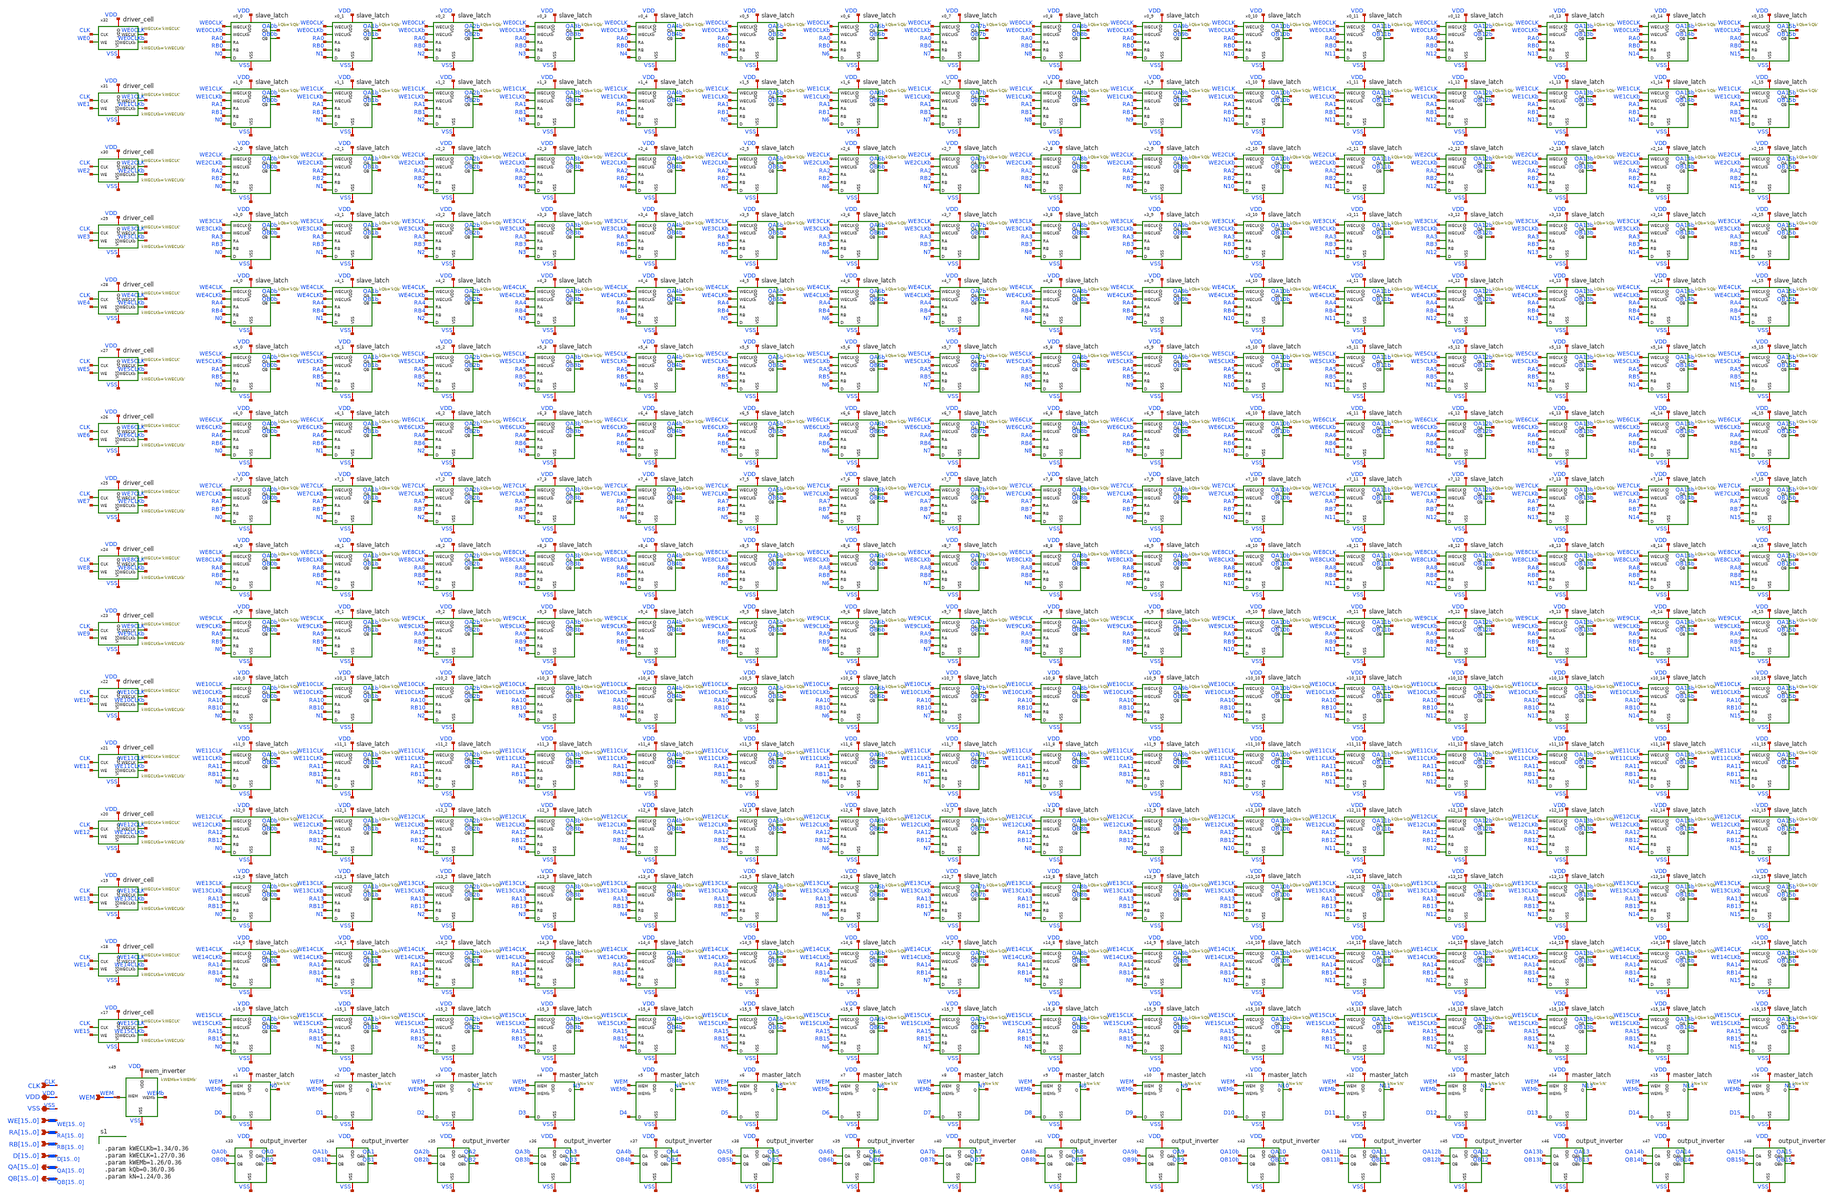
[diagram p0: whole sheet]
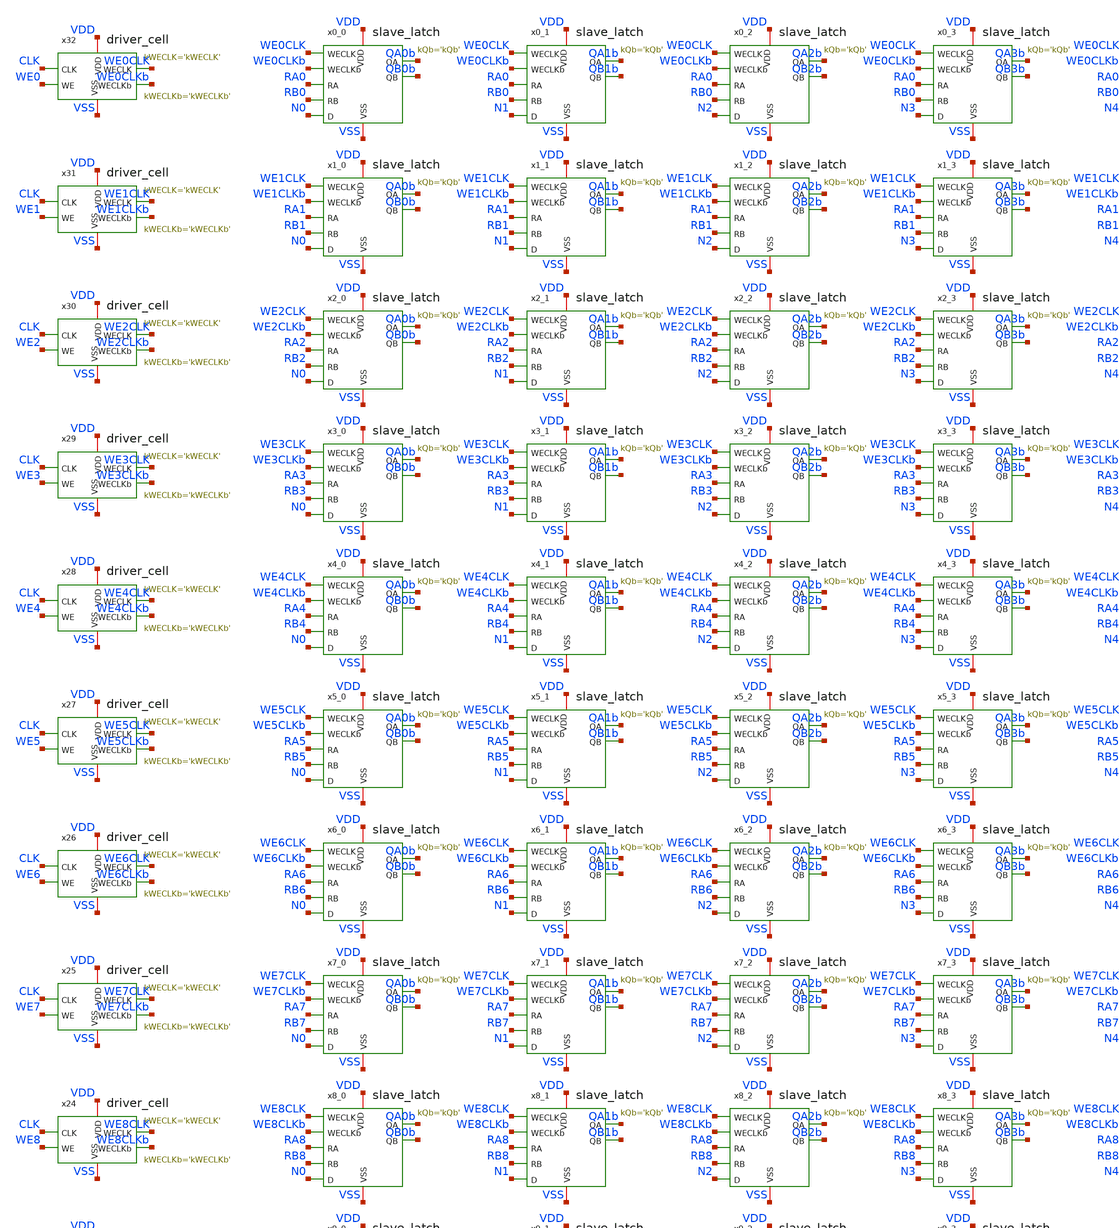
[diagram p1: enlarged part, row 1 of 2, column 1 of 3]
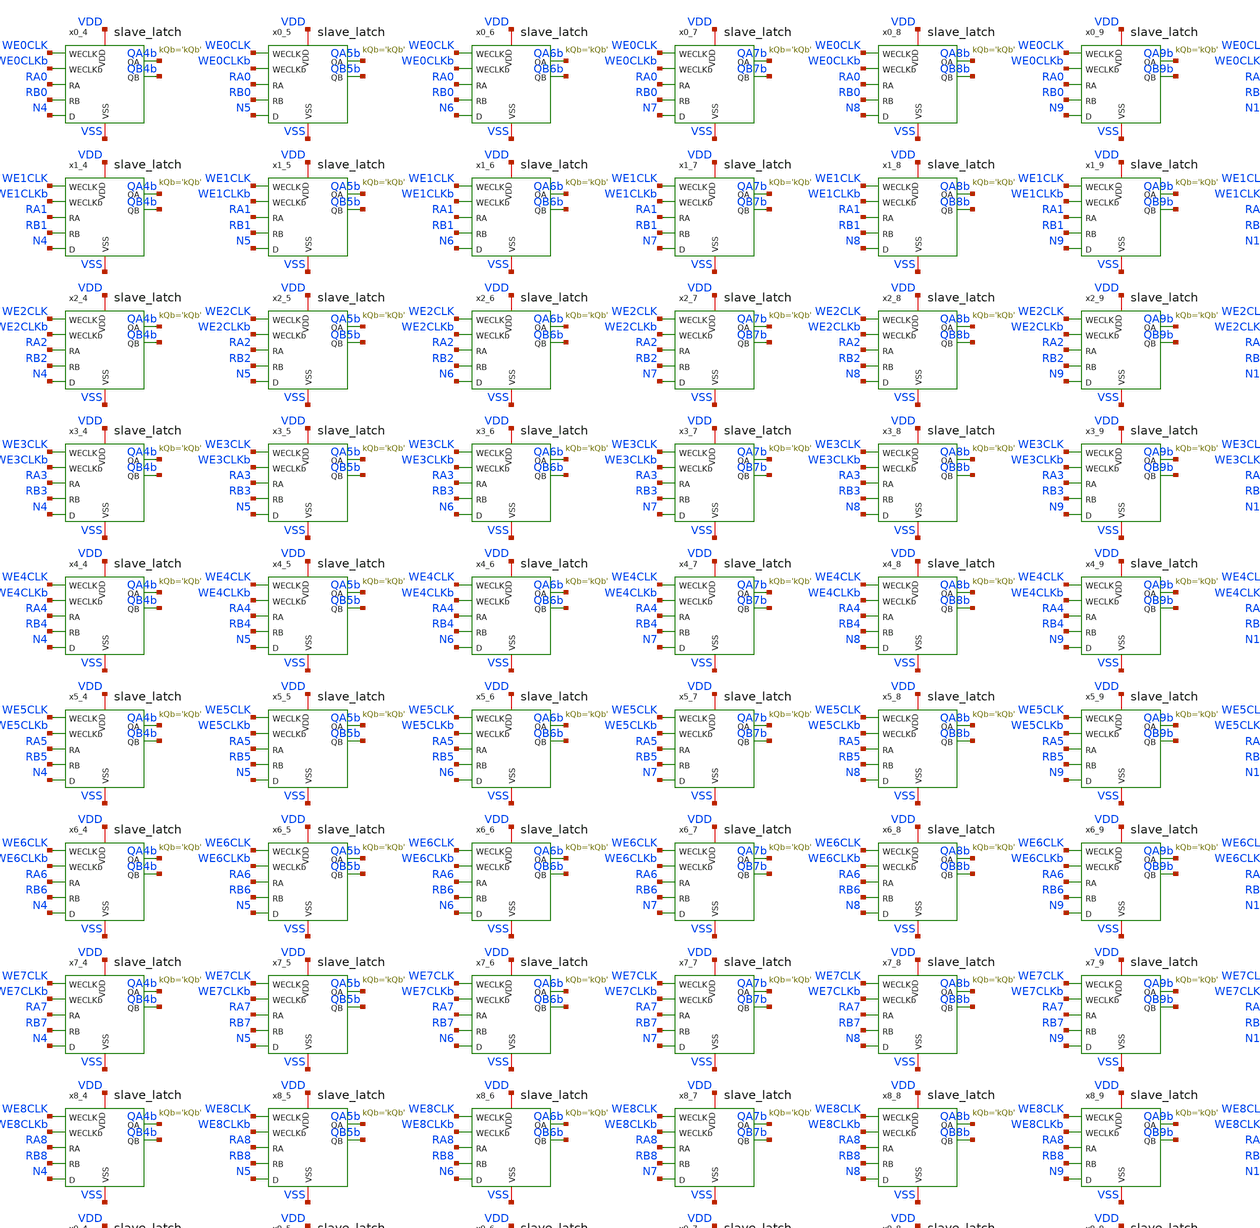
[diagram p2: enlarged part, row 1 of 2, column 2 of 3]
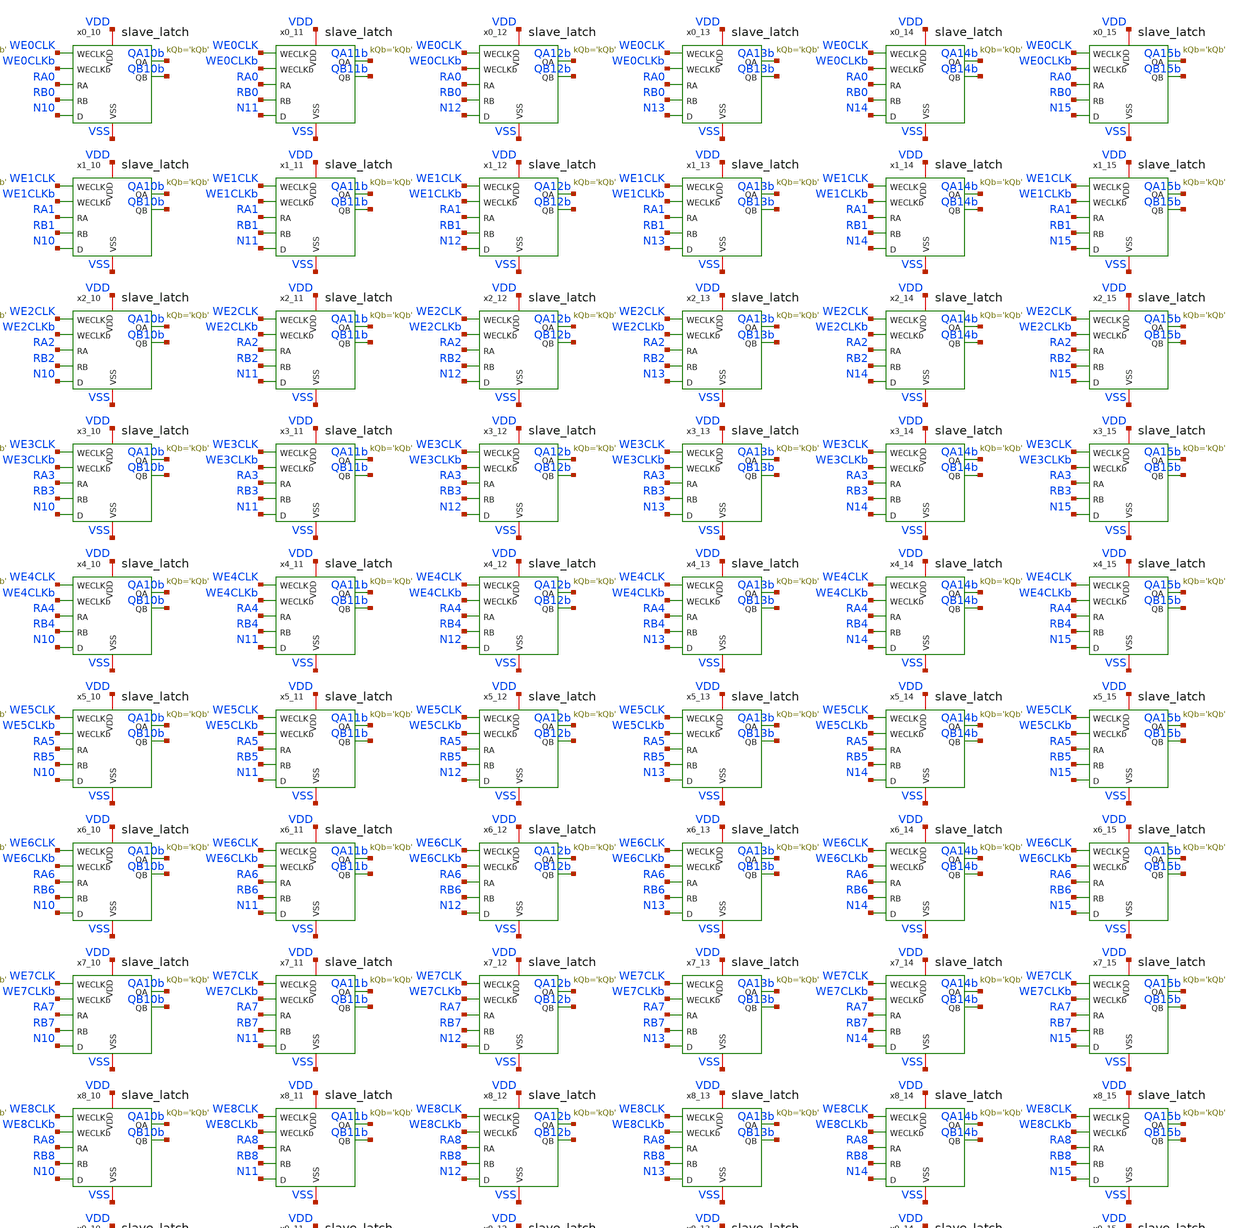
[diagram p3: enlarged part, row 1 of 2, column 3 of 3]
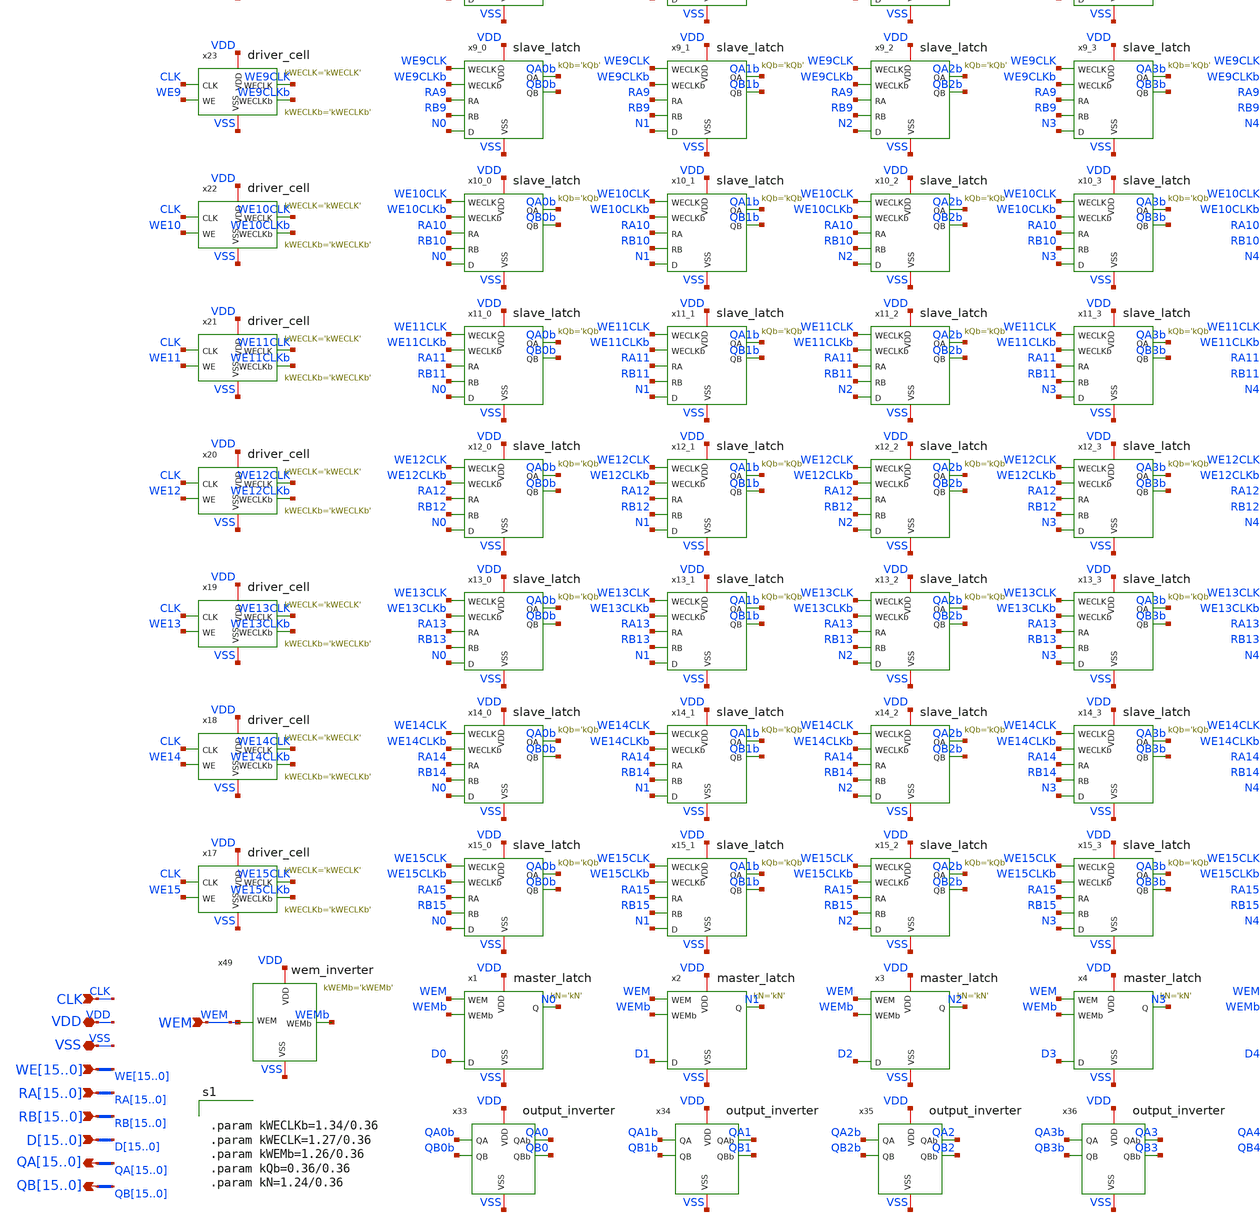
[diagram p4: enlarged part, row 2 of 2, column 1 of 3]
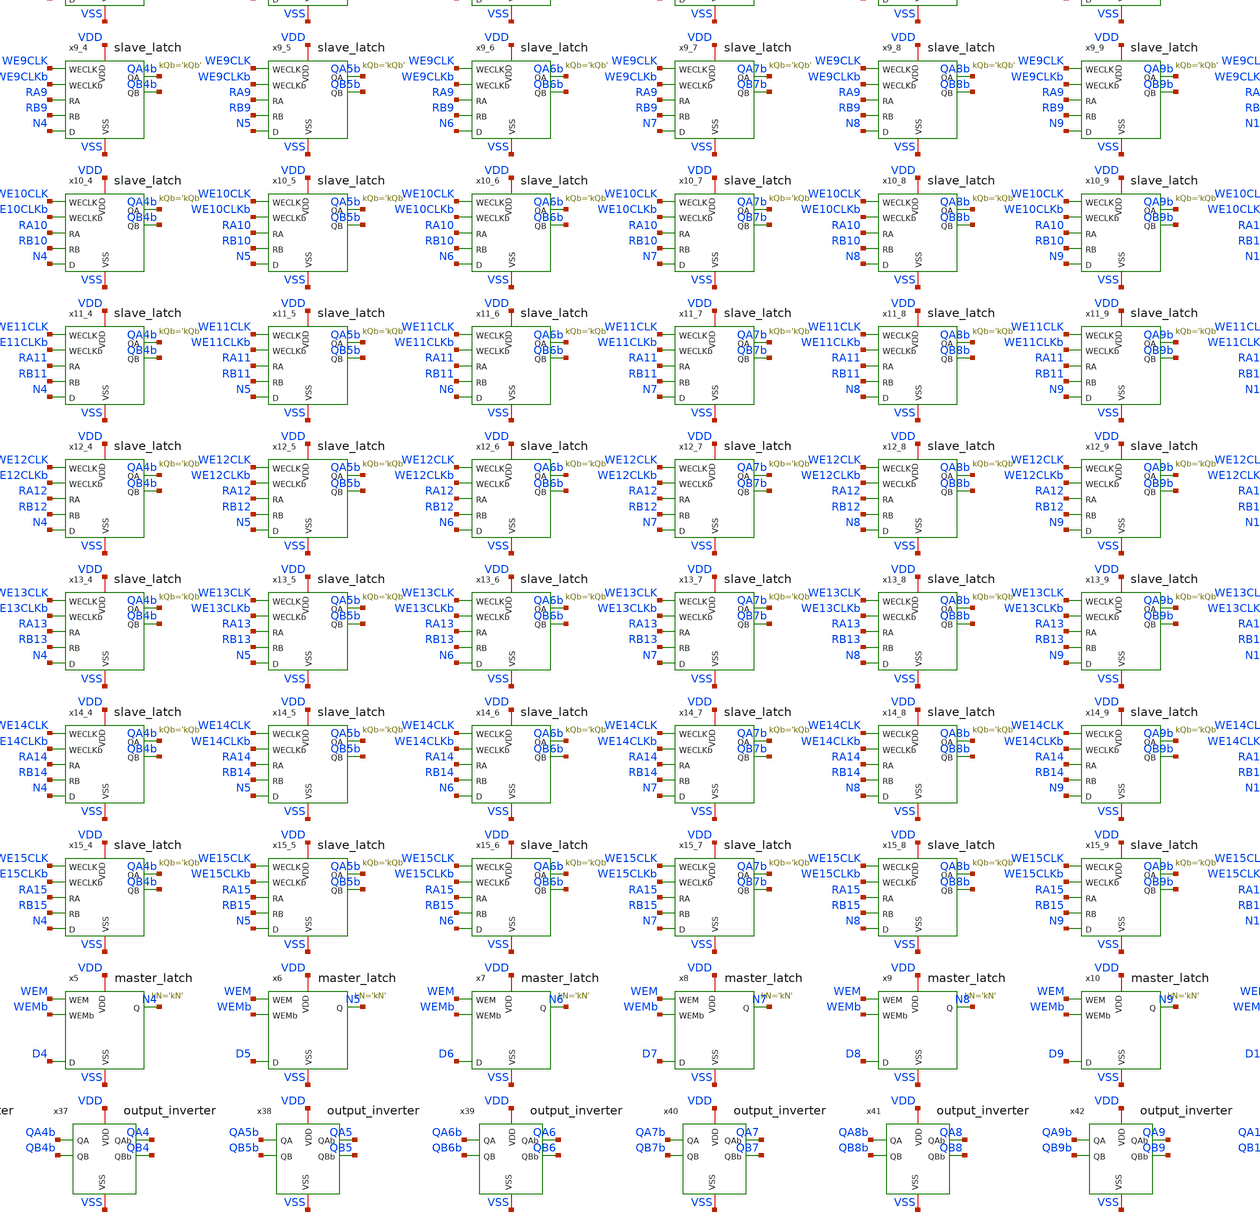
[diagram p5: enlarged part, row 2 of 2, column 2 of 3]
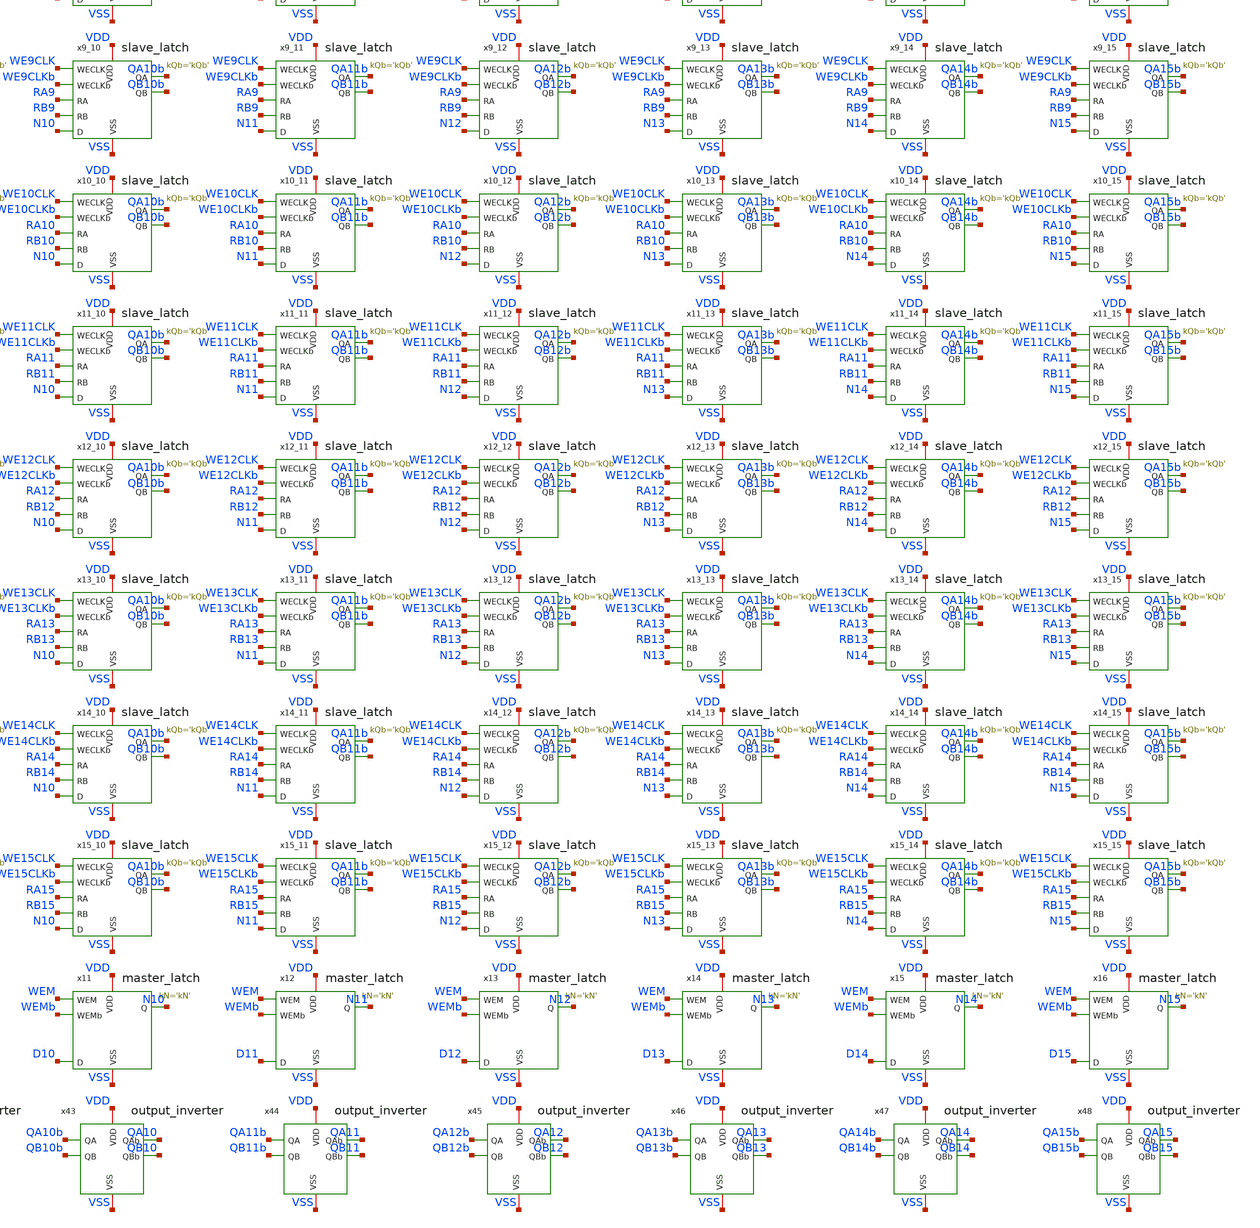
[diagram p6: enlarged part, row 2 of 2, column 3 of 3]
** sch_path: CAD3/rf.sch
**.subckt rf RA15,RA14,RA13,RA12,RA11,RA10,RA9,RA8,RA7,RA6,RA5,RA4,RA3,RA2,RA1,RA0
*+ RB15,RB14,RB13,RB12,RB11,RB10,RB9,RB8,RB7,RB6,RB5,RB4,RB3,RB2,RB1,RB0 WE15,WE14,WE13,WE12,WE11,WE10,WE9,WE8,WE7,WE6,WE5,WE4,WE3,WE2,WE1,WE0 CLK WEM
*+ D15,D14,D13,D12,D11,D10,D9,D8,D7,D6,D5,D4,D3,D2,D1,D0 VDD VSS QA15,QA14,QA13,QA12,QA11,QA10,QA9,QA8,QA7,QA6,QA5,QA4,QA3,QA2,QA1,QA0
*+ QB15,QB14,QB13,QB12,QB11,QB10,QB9,QB8,QB7,QB6,QB5,QB4,QB3,QB2,QB1,QB0
*.ipin RA15,RA14,RA13,RA12,RA11,RA10,RA9,RA8,RA7,RA6,RA5,RA4,RA3,RA2,RA1,RA0
*.ipin RB15,RB14,RB13,RB12,RB11,RB10,RB9,RB8,RB7,RB6,RB5,RB4,RB3,RB2,RB1,RB0
*.ipin WE15,WE14,WE13,WE12,WE11,WE10,WE9,WE8,WE7,WE6,WE5,WE4,WE3,WE2,WE1,WE0
*.ipin CLK
*.ipin WEM
*.ipin D15,D14,D13,D12,D11,D10,D9,D8,D7,D6,D5,D4,D3,D2,D1,D0
*.iopin VDD
*.iopin VSS
*.opin QA15,QA14,QA13,QA12,QA11,QA10,QA9,QA8,QA7,QA6,QA5,QA4,QA3,QA2,QA1,QA0
*.opin QB15,QB14,QB13,QB12,QB11,QB10,QB9,QB8,QB7,QB6,QB5,QB4,QB3,QB2,QB1,QB0
x0_0 VDD VSS QA0b WE0CLK WE0CLKb RA0 RB0 QB0b N0 slave_latch kQb='kQb'
x0_1 VDD VSS QA1b WE0CLK WE0CLKb RA0 RB0 QB1b N1 slave_latch kQb='kQb'
x0_2 VDD VSS QA2b WE0CLK WE0CLKb RA0 RB0 QB2b N2 slave_latch kQb='kQb'
x0_3 VDD VSS QA3b WE0CLK WE0CLKb RA0 RB0 QB3b N3 slave_latch kQb='kQb'
x0_4 VDD VSS QA4b WE0CLK WE0CLKb RA0 RB0 QB4b N4 slave_latch kQb='kQb'
x0_5 VDD VSS QA5b WE0CLK WE0CLKb RA0 RB0 QB5b N5 slave_latch kQb='kQb'
x0_6 VDD VSS QA6b WE0CLK WE0CLKb RA0 RB0 QB6b N6 slave_latch kQb='kQb'
x0_7 VDD VSS QA7b WE0CLK WE0CLKb RA0 RB0 QB7b N7 slave_latch kQb='kQb'
x0_8 VDD VSS QA8b WE0CLK WE0CLKb RA0 RB0 QB8b N8 slave_latch kQb='kQb'
x0_9 VDD VSS QA9b WE0CLK WE0CLKb RA0 RB0 QB9b N9 slave_latch kQb='kQb'
x0_10 VDD VSS QA10b WE0CLK WE0CLKb RA0 RB0 QB10b N10 slave_latch kQb='kQb'
x0_11 VDD VSS QA11b WE0CLK WE0CLKb RA0 RB0 QB11b N11 slave_latch kQb='kQb'
x0_12 VDD VSS QA12b WE0CLK WE0CLKb RA0 RB0 QB12b N12 slave_latch kQb='kQb'
x0_13 VDD VSS QA13b WE0CLK WE0CLKb RA0 RB0 QB13b N13 slave_latch kQb='kQb'
x0_14 VDD VSS QA14b WE0CLK WE0CLKb RA0 RB0 QB14b N14 slave_latch kQb='kQb'
x0_15 VDD VSS QA15b WE0CLK WE0CLKb RA0 RB0 QB15b N15 slave_latch kQb='kQb'
x1_0 VDD VSS QA0b WE1CLK WE1CLKb RA1 RB1 QB0b N0 slave_latch kQb='kQb'
x1_1 VDD VSS QA1b WE1CLK WE1CLKb RA1 RB1 QB1b N1 slave_latch kQb='kQb'
x1_2 VDD VSS QA2b WE1CLK WE1CLKb RA1 RB1 QB2b N2 slave_latch kQb='kQb'
x1_3 VDD VSS QA3b WE1CLK WE1CLKb RA1 RB1 QB3b N3 slave_latch kQb='kQb'
x1_4 VDD VSS QA4b WE1CLK WE1CLKb RA1 RB1 QB4b N4 slave_latch kQb='kQb'
x1_5 VDD VSS QA5b WE1CLK WE1CLKb RA1 RB1 QB5b N5 slave_latch kQb='kQb'
x1_6 VDD VSS QA6b WE1CLK WE1CLKb RA1 RB1 QB6b N6 slave_latch kQb='kQb'
x1_7 VDD VSS QA7b WE1CLK WE1CLKb RA1 RB1 QB7b N7 slave_latch kQb='kQb'
x1_8 VDD VSS QA8b WE1CLK WE1CLKb RA1 RB1 QB8b N8 slave_latch kQb='kQb'
x1_9 VDD VSS QA9b WE1CLK WE1CLKb RA1 RB1 QB9b N9 slave_latch kQb='kQb'
x1_10 VDD VSS QA10b WE1CLK WE1CLKb RA1 RB1 QB10b N10 slave_latch kQb='kQb'
x1_11 VDD VSS QA11b WE1CLK WE1CLKb RA1 RB1 QB11b N11 slave_latch kQb='kQb'
x1_12 VDD VSS QA12b WE1CLK WE1CLKb RA1 RB1 QB12b N12 slave_latch kQb='kQb'
x1_13 VDD VSS QA13b WE1CLK WE1CLKb RA1 RB1 QB13b N13 slave_latch kQb='kQb'
x1_14 VDD VSS QA14b WE1CLK WE1CLKb RA1 RB1 QB14b N14 slave_latch kQb='kQb'
x1_15 VDD VSS QA15b WE1CLK WE1CLKb RA1 RB1 QB15b N15 slave_latch kQb='kQb'
x2_0 VDD VSS QA0b WE2CLK WE2CLKb RA2 RB2 QB0b N0 slave_latch kQb='kQb'
x2_1 VDD VSS QA1b WE2CLK WE2CLKb RA2 RB2 QB1b N1 slave_latch kQb='kQb'
x2_2 VDD VSS QA2b WE2CLK WE2CLKb RA2 RB2 QB2b N2 slave_latch kQb='kQb'
x2_3 VDD VSS QA3b WE2CLK WE2CLKb RA2 RB2 QB3b N3 slave_latch kQb='kQb'
x2_4 VDD VSS QA4b WE2CLK WE2CLKb RA2 RB2 QB4b N4 slave_latch kQb='kQb'
x2_5 VDD VSS QA5b WE2CLK WE2CLKb RA2 RB2 QB5b N5 slave_latch kQb='kQb'
x2_6 VDD VSS QA6b WE2CLK WE2CLKb RA2 RB2 QB6b N6 slave_latch kQb='kQb'
x2_7 VDD VSS QA7b WE2CLK WE2CLKb RA2 RB2 QB7b N7 slave_latch kQb='kQb'
x2_8 VDD VSS QA8b WE2CLK WE2CLKb RA2 RB2 QB8b N8 slave_latch kQb='kQb'
x2_9 VDD VSS QA9b WE2CLK WE2CLKb RA2 RB2 QB9b N9 slave_latch kQb='kQb'
x2_10 VDD VSS QA10b WE2CLK WE2CLKb RA2 RB2 QB10b N10 slave_latch kQb='kQb'
x2_11 VDD VSS QA11b WE2CLK WE2CLKb RA2 RB2 QB11b N11 slave_latch kQb='kQb'
x2_12 VDD VSS QA12b WE2CLK WE2CLKb RA2 RB2 QB12b N12 slave_latch kQb='kQb'
x2_13 VDD VSS QA13b WE2CLK WE2CLKb RA2 RB2 QB13b N13 slave_latch kQb='kQb'
x2_14 VDD VSS QA14b WE2CLK WE2CLKb RA2 RB2 QB14b N14 slave_latch kQb='kQb'
x2_15 VDD VSS QA15b WE2CLK WE2CLKb RA2 RB2 QB15b N15 slave_latch kQb='kQb'
x3_0 VDD VSS QA0b WE3CLK WE3CLKb RA3 RB3 QB0b N0 slave_latch kQb='kQb'
x3_1 VDD VSS QA1b WE3CLK WE3CLKb RA3 RB3 QB1b N1 slave_latch kQb='kQb'
x3_2 VDD VSS QA2b WE3CLK WE3CLKb RA3 RB3 QB2b N2 slave_latch kQb='kQb'
x3_3 VDD VSS QA3b WE3CLK WE3CLKb RA3 RB3 QB3b N3 slave_latch kQb='kQb'
x3_4 VDD VSS QA4b WE3CLK WE3CLKb RA3 RB3 QB4b N4 slave_latch kQb='kQb'
x3_5 VDD VSS QA5b WE3CLK WE3CLKb RA3 RB3 QB5b N5 slave_latch kQb='kQb'
x3_6 VDD VSS QA6b WE3CLK WE3CLKb RA3 RB3 QB6b N6 slave_latch kQb='kQb'
x3_7 VDD VSS QA7b WE3CLK WE3CLKb RA3 RB3 QB7b N7 slave_latch kQb='kQb'
x3_8 VDD VSS QA8b WE3CLK WE3CLKb RA3 RB3 QB8b N8 slave_latch kQb='kQb'
x3_9 VDD VSS QA9b WE3CLK WE3CLKb RA3 RB3 QB9b N9 slave_latch kQb='kQb'
x3_10 VDD VSS QA10b WE3CLK WE3CLKb RA3 RB3 QB10b N10 slave_latch kQb='kQb'
x3_11 VDD VSS QA11b WE3CLK WE3CLKb RA3 RB3 QB11b N11 slave_latch kQb='kQb'
x3_12 VDD VSS QA12b WE3CLK WE3CLKb RA3 RB3 QB12b N12 slave_latch kQb='kQb'
x3_13 VDD VSS QA13b WE3CLK WE3CLKb RA3 RB3 QB13b N13 slave_latch kQb='kQb'
x3_14 VDD VSS QA14b WE3CLK WE3CLKb RA3 RB3 QB14b N14 slave_latch kQb='kQb'
x3_15 VDD VSS QA15b WE3CLK WE3CLKb RA3 RB3 QB15b N15 slave_latch kQb='kQb'
x4_0 VDD VSS QA0b WE4CLK WE4CLKb RA4 RB4 QB0b N0 slave_latch kQb='kQb'
x4_1 VDD VSS QA1b WE4CLK WE4CLKb RA4 RB4 QB1b N1 slave_latch kQb='kQb'
x4_2 VDD VSS QA2b WE4CLK WE4CLKb RA4 RB4 QB2b N2 slave_latch kQb='kQb'
x4_3 VDD VSS QA3b WE4CLK WE4CLKb RA4 RB4 QB3b N3 slave_latch kQb='kQb'
x4_4 VDD VSS QA4b WE4CLK WE4CLKb RA4 RB4 QB4b N4 slave_latch kQb='kQb'
x4_5 VDD VSS QA5b WE4CLK WE4CLKb RA4 RB4 QB5b N5 slave_latch kQb='kQb'
x4_6 VDD VSS QA6b WE4CLK WE4CLKb RA4 RB4 QB6b N6 slave_latch kQb='kQb'
x4_7 VDD VSS QA7b WE4CLK WE4CLKb RA4 RB4 QB7b N7 slave_latch kQb='kQb'
x4_8 VDD VSS QA8b WE4CLK WE4CLKb RA4 RB4 QB8b N8 slave_latch kQb='kQb'
x4_9 VDD VSS QA9b WE4CLK WE4CLKb RA4 RB4 QB9b N9 slave_latch kQb='kQb'
x4_10 VDD VSS QA10b WE4CLK WE4CLKb RA4 RB4 QB10b N10 slave_latch kQb='kQb'
x4_11 VDD VSS QA11b WE4CLK WE4CLKb RA4 RB4 QB11b N11 slave_latch kQb='kQb'
x4_12 VDD VSS QA12b WE4CLK WE4CLKb RA4 RB4 QB12b N12 slave_latch kQb='kQb'
x4_13 VDD VSS QA13b WE4CLK WE4CLKb RA4 RB4 QB13b N13 slave_latch kQb='kQb'
x4_14 VDD VSS QA14b WE4CLK WE4CLKb RA4 RB4 QB14b N14 slave_latch kQb='kQb'
x4_15 VDD VSS QA15b WE4CLK WE4CLKb RA4 RB4 QB15b N15 slave_latch kQb='kQb'
x5_0 VDD VSS QA0b WE5CLK WE5CLKb RA5 RB5 QB0b N0 slave_latch kQb='kQb'
x5_1 VDD VSS QA1b WE5CLK WE5CLKb RA5 RB5 QB1b N1 slave_latch kQb='kQb'
x5_2 VDD VSS QA2b WE5CLK WE5CLKb RA5 RB5 QB2b N2 slave_latch kQb='kQb'
x5_3 VDD VSS QA3b WE5CLK WE5CLKb RA5 RB5 QB3b N3 slave_latch kQb='kQb'
x5_4 VDD VSS QA4b WE5CLK WE5CLKb RA5 RB5 QB4b N4 slave_latch kQb='kQb'
x5_5 VDD VSS QA5b WE5CLK WE5CLKb RA5 RB5 QB5b N5 slave_latch kQb='kQb'
x5_6 VDD VSS QA6b WE5CLK WE5CLKb RA5 RB5 QB6b N6 slave_latch kQb='kQb'
x5_7 VDD VSS QA7b WE5CLK WE5CLKb RA5 RB5 QB7b N7 slave_latch kQb='kQb'
x5_8 VDD VSS QA8b WE5CLK WE5CLKb RA5 RB5 QB8b N8 slave_latch kQb='kQb'
x5_9 VDD VSS QA9b WE5CLK WE5CLKb RA5 RB5 QB9b N9 slave_latch kQb='kQb'
x5_10 VDD VSS QA10b WE5CLK WE5CLKb RA5 RB5 QB10b N10 slave_latch kQb='kQb'
x5_11 VDD VSS QA11b WE5CLK WE5CLKb RA5 RB5 QB11b N11 slave_latch kQb='kQb'
x5_12 VDD VSS QA12b WE5CLK WE5CLKb RA5 RB5 QB12b N12 slave_latch kQb='kQb'
x5_13 VDD VSS QA13b WE5CLK WE5CLKb RA5 RB5 QB13b N13 slave_latch kQb='kQb'
x5_14 VDD VSS QA14b WE5CLK WE5CLKb RA5 RB5 QB14b N14 slave_latch kQb='kQb'
x5_15 VDD VSS QA15b WE5CLK WE5CLKb RA5 RB5 QB15b N15 slave_latch kQb='kQb'
x6_0 VDD VSS QA0b WE6CLK WE6CLKb RA6 RB6 QB0b N0 slave_latch kQb='kQb'
x6_1 VDD VSS QA1b WE6CLK WE6CLKb RA6 RB6 QB1b N1 slave_latch kQb='kQb'
x6_2 VDD VSS QA2b WE6CLK WE6CLKb RA6 RB6 QB2b N2 slave_latch kQb='kQb'
x6_3 VDD VSS QA3b WE6CLK WE6CLKb RA6 RB6 QB3b N3 slave_latch kQb='kQb'
x6_4 VDD VSS QA4b WE6CLK WE6CLKb RA6 RB6 QB4b N4 slave_latch kQb='kQb'
x6_5 VDD VSS QA5b WE6CLK WE6CLKb RA6 RB6 QB5b N5 slave_latch kQb='kQb'
x6_6 VDD VSS QA6b WE6CLK WE6CLKb RA6 RB6 QB6b N6 slave_latch kQb='kQb'
x6_7 VDD VSS QA7b WE6CLK WE6CLKb RA6 RB6 QB7b N7 slave_latch kQb='kQb'
x6_8 VDD VSS QA8b WE6CLK WE6CLKb RA6 RB6 QB8b N8 slave_latch kQb='kQb'
x6_9 VDD VSS QA9b WE6CLK WE6CLKb RA6 RB6 QB9b N9 slave_latch kQb='kQb'
x6_10 VDD VSS QA10b WE6CLK WE6CLKb RA6 RB6 QB10b N10 slave_latch kQb='kQb'
x6_11 VDD VSS QA11b WE6CLK WE6CLKb RA6 RB6 QB11b N11 slave_latch kQb='kQb'
x6_12 VDD VSS QA12b WE6CLK WE6CLKb RA6 RB6 QB12b N12 slave_latch kQb='kQb'
x6_13 VDD VSS QA13b WE6CLK WE6CLKb RA6 RB6 QB13b N13 slave_latch kQb='kQb'
x6_14 VDD VSS QA14b WE6CLK WE6CLKb RA6 RB6 QB14b N14 slave_latch kQb='kQb'
x6_15 VDD VSS QA15b WE6CLK WE6CLKb RA6 RB6 QB15b N15 slave_latch kQb='kQb'
x7_0 VDD VSS QA0b WE7CLK WE7CLKb RA7 RB7 QB0b N0 slave_latch kQb='kQb'
x7_1 VDD VSS QA1b WE7CLK WE7CLKb RA7 RB7 QB1b N1 slave_latch kQb='kQb'
x7_2 VDD VSS QA2b WE7CLK WE7CLKb RA7 RB7 QB2b N2 slave_latch kQb='kQb'
x7_3 VDD VSS QA3b WE7CLK WE7CLKb RA7 RB7 QB3b N3 slave_latch kQb='kQb'
x7_4 VDD VSS QA4b WE7CLK WE7CLKb RA7 RB7 QB4b N4 slave_latch kQb='kQb'
x7_5 VDD VSS QA5b WE7CLK WE7CLKb RA7 RB7 QB5b N5 slave_latch kQb='kQb'
x7_6 VDD VSS QA6b WE7CLK WE7CLKb RA7 RB7 QB6b N6 slave_latch kQb='kQb'
x7_7 VDD VSS QA7b WE7CLK WE7CLKb RA7 RB7 QB7b N7 slave_latch kQb='kQb'
x7_8 VDD VSS QA8b WE7CLK WE7CLKb RA7 RB7 QB8b N8 slave_latch kQb='kQb'
x7_9 VDD VSS QA9b WE7CLK WE7CLKb RA7 RB7 QB9b N9 slave_latch kQb='kQb'
x7_10 VDD VSS QA10b WE7CLK WE7CLKb RA7 RB7 QB10b N10 slave_latch kQb='kQb'
x7_11 VDD VSS QA11b WE7CLK WE7CLKb RA7 RB7 QB11b N11 slave_latch kQb='kQb'
x7_12 VDD VSS QA12b WE7CLK WE7CLKb RA7 RB7 QB12b N12 slave_latch kQb='kQb'
x7_13 VDD VSS QA13b WE7CLK WE7CLKb RA7 RB7 QB13b N13 slave_latch kQb='kQb'
x7_14 VDD VSS QA14b WE7CLK WE7CLKb RA7 RB7 QB14b N14 slave_latch kQb='kQb'
x7_15 VDD VSS QA15b WE7CLK WE7CLKb RA7 RB7 QB15b N15 slave_latch kQb='kQb'
x8_0 VDD VSS QA0b WE8CLK WE8CLKb RA8 RB8 QB0b N0 slave_latch kQb='kQb'
x8_1 VDD VSS QA1b WE8CLK WE8CLKb RA8 RB8 QB1b N1 slave_latch kQb='kQb'
x8_2 VDD VSS QA2b WE8CLK WE8CLKb RA8 RB8 QB2b N2 slave_latch kQb='kQb'
x8_3 VDD VSS QA3b WE8CLK WE8CLKb RA8 RB8 QB3b N3 slave_latch kQb='kQb'
x8_4 VDD VSS QA4b WE8CLK WE8CLKb RA8 RB8 QB4b N4 slave_latch kQb='kQb'
x8_5 VDD VSS QA5b WE8CLK WE8CLKb RA8 RB8 QB5b N5 slave_latch kQb='kQb'
x8_6 VDD VSS QA6b WE8CLK WE8CLKb RA8 RB8 QB6b N6 slave_latch kQb='kQb'
x8_7 VDD VSS QA7b WE8CLK WE8CLKb RA8 RB8 QB7b N7 slave_latch kQb='kQb'
x8_8 VDD VSS QA8b WE8CLK WE8CLKb RA8 RB8 QB8b N8 slave_latch kQb='kQb'
x8_9 VDD VSS QA9b WE8CLK WE8CLKb RA8 RB8 QB9b N9 slave_latch kQb='kQb'
x8_10 VDD VSS QA10b WE8CLK WE8CLKb RA8 RB8 QB10b N10 slave_latch kQb='kQb'
x8_11 VDD VSS QA11b WE8CLK WE8CLKb RA8 RB8 QB11b N11 slave_latch kQb='kQb'
x8_12 VDD VSS QA12b WE8CLK WE8CLKb RA8 RB8 QB12b N12 slave_latch kQb='kQb'
x8_13 VDD VSS QA13b WE8CLK WE8CLKb RA8 RB8 QB13b N13 slave_latch kQb='kQb'
x8_14 VDD VSS QA14b WE8CLK WE8CLKb RA8 RB8 QB14b N14 slave_latch kQb='kQb'
x8_15 VDD VSS QA15b WE8CLK WE8CLKb RA8 RB8 QB15b N15 slave_latch kQb='kQb'
x9_0 VDD VSS QA0b WE9CLK WE9CLKb RA9 RB9 QB0b N0 slave_latch kQb='kQb'
x9_1 VDD VSS QA1b WE9CLK WE9CLKb RA9 RB9 QB1b N1 slave_latch kQb='kQb'
x9_2 VDD VSS QA2b WE9CLK WE9CLKb RA9 RB9 QB2b N2 slave_latch kQb='kQb'
x9_3 VDD VSS QA3b WE9CLK WE9CLKb RA9 RB9 QB3b N3 slave_latch kQb='kQb'
x9_4 VDD VSS QA4b WE9CLK WE9CLKb RA9 RB9 QB4b N4 slave_latch kQb='kQb'
x9_5 VDD VSS QA5b WE9CLK WE9CLKb RA9 RB9 QB5b N5 slave_latch kQb='kQb'
x9_6 VDD VSS QA6b WE9CLK WE9CLKb RA9 RB9 QB6b N6 slave_latch kQb='kQb'
x9_7 VDD VSS QA7b WE9CLK WE9CLKb RA9 RB9 QB7b N7 slave_latch kQb='kQb'
x9_8 VDD VSS QA8b WE9CLK WE9CLKb RA9 RB9 QB8b N8 slave_latch kQb='kQb'
x9_9 VDD VSS QA9b WE9CLK WE9CLKb RA9 RB9 QB9b N9 slave_latch kQb='kQb'
x9_10 VDD VSS QA10b WE9CLK WE9CLKb RA9 RB9 QB10b N10 slave_latch kQb='kQb'
x9_11 VDD VSS QA11b WE9CLK WE9CLKb RA9 RB9 QB11b N11 slave_latch kQb='kQb'
x9_12 VDD VSS QA12b WE9CLK WE9CLKb RA9 RB9 QB12b N12 slave_latch kQb='kQb'
x9_13 VDD VSS QA13b WE9CLK WE9CLKb RA9 RB9 QB13b N13 slave_latch kQb='kQb'
x9_14 VDD VSS QA14b WE9CLK WE9CLKb RA9 RB9 QB14b N14 slave_latch kQb='kQb'
x9_15 VDD VSS QA15b WE9CLK WE9CLKb RA9 RB9 QB15b N15 slave_latch kQb='kQb'
x10_0 VDD VSS QA0b WE10CLK WE10CLKb RA10 RB10 QB0b N0 slave_latch kQb='kQb'
x10_1 VDD VSS QA1b WE10CLK WE10CLKb RA10 RB10 QB1b N1 slave_latch kQb='kQb'
x10_2 VDD VSS QA2b WE10CLK WE10CLKb RA10 RB10 QB2b N2 slave_latch kQb='kQb'
x10_3 VDD VSS QA3b WE10CLK WE10CLKb RA10 RB10 QB3b N3 slave_latch kQb='kQb'
x10_4 VDD VSS QA4b WE10CLK WE10CLKb RA10 RB10 QB4b N4 slave_latch kQb='kQb'
x10_5 VDD VSS QA5b WE10CLK WE10CLKb RA10 RB10 QB5b N5 slave_latch kQb='kQb'
x10_6 VDD VSS QA6b WE10CLK WE10CLKb RA10 RB10 QB6b N6 slave_latch kQb='kQb'
x10_7 VDD VSS QA7b WE10CLK WE10CLKb RA10 RB10 QB7b N7 slave_latch kQb='kQb'
x10_8 VDD VSS QA8b WE10CLK WE10CLKb RA10 RB10 QB8b N8 slave_latch kQb='kQb'
x10_9 VDD VSS QA9b WE10CLK WE10CLKb RA10 RB10 QB9b N9 slave_latch kQb='kQb'
x10_10 VDD VSS QA10b WE10CLK WE10CLKb RA10 RB10 QB10b N10 slave_latch kQb='kQb'
x10_11 VDD VSS QA11b WE10CLK WE10CLKb RA10 RB10 QB11b N11 slave_latch kQb='kQb'
x10_12 VDD VSS QA12b WE10CLK WE10CLKb RA10 RB10 QB12b N12 slave_latch kQb='kQb'
x10_13 VDD VSS QA13b WE10CLK WE10CLKb RA10 RB10 QB13b N13 slave_latch kQb='kQb'
x10_14 VDD VSS QA14b WE10CLK WE10CLKb RA10 RB10 QB14b N14 slave_latch kQb='kQb'
x10_15 VDD VSS QA15b WE10CLK WE10CLKb RA10 RB10 QB15b N15 slave_latch kQb='kQb'
x11_0 VDD VSS QA0b WE11CLK WE11CLKb RA11 RB11 QB0b N0 slave_latch kQb='kQb'
x11_1 VDD VSS QA1b WE11CLK WE11CLKb RA11 RB11 QB1b N1 slave_latch kQb='kQb'
x11_2 VDD VSS QA2b WE11CLK WE11CLKb RA11 RB11 QB2b N2 slave_latch kQb='kQb'
x11_3 VDD VSS QA3b WE11CLK WE11CLKb RA11 RB11 QB3b N3 slave_latch kQb='kQb'
x11_4 VDD VSS QA4b WE11CLK WE11CLKb RA11 RB11 QB4b N4 slave_latch kQb='kQb'
x11_5 VDD VSS QA5b WE11CLK WE11CLKb RA11 RB11 QB5b N5 slave_latch kQb='kQb'
x11_6 VDD VSS QA6b WE11CLK WE11CLKb RA11 RB11 QB6b N6 slave_latch kQb='kQb'
x11_7 VDD VSS QA7b WE11CLK WE11CLKb RA11 RB11 QB7b N7 slave_latch kQb='kQb'
x11_8 VDD VSS QA8b WE11CLK WE11CLKb RA11 RB11 QB8b N8 slave_latch kQb='kQb'
x11_9 VDD VSS QA9b WE11CLK WE11CLKb RA11 RB11 QB9b N9 slave_latch kQb='kQb'
x11_10 VDD VSS QA10b WE11CLK WE11CLKb RA11 RB11 QB10b N10 slave_latch kQb='kQb'
x11_11 VDD VSS QA11b WE11CLK WE11CLKb RA11 RB11 QB11b N11 slave_latch kQb='kQb'
x11_12 VDD VSS QA12b WE11CLK WE11CLKb RA11 RB11 QB12b N12 slave_latch kQb='kQb'
x11_13 VDD VSS QA13b WE11CLK WE11CLKb RA11 RB11 QB13b N13 slave_latch kQb='kQb'
x11_14 VDD VSS QA14b WE11CLK WE11CLKb RA11 RB11 QB14b N14 slave_latch kQb='kQb'
x11_15 VDD VSS QA15b WE11CLK WE11CLKb RA11 RB11 QB15b N15 slave_latch kQb='kQb'
x12_0 VDD VSS QA0b WE12CLK WE12CLKb RA12 RB12 QB0b N0 slave_latch kQb='kQb'
x12_1 VDD VSS QA1b WE12CLK WE12CLKb RA12 RB12 QB1b N1 slave_latch kQb='kQb'
x12_2 VDD VSS QA2b WE12CLK WE12CLKb RA12 RB12 QB2b N2 slave_latch kQb='kQb'
x12_3 VDD VSS QA3b WE12CLK WE12CLKb RA12 RB12 QB3b N3 slave_latch kQb='kQb'
x12_4 VDD VSS QA4b WE12CLK WE12CLKb RA12 RB12 QB4b N4 slave_latch kQb='kQb'
x12_5 VDD VSS QA5b WE12CLK WE12CLKb RA12 RB12 QB5b N5 slave_latch kQb='kQb'
x12_6 VDD VSS QA6b WE12CLK WE12CLKb RA12 RB12 QB6b N6 slave_latch kQb='kQb'
x12_7 VDD VSS QA7b WE12CLK WE12CLKb RA12 RB12 QB7b N7 slave_latch kQb='kQb'
x12_8 VDD VSS QA8b WE12CLK WE12CLKb RA12 RB12 QB8b N8 slave_latch kQb='kQb'
x12_9 VDD VSS QA9b WE12CLK WE12CLKb RA12 RB12 QB9b N9 slave_latch kQb='kQb'
x12_10 VDD VSS QA10b WE12CLK WE12CLKb RA12 RB12 QB10b N10 slave_latch kQb='kQb'
x12_11 VDD VSS QA11b WE12CLK WE12CLKb RA12 RB12 QB11b N11 slave_latch kQb='kQb'
x12_12 VDD VSS QA12b WE12CLK WE12CLKb RA12 RB12 QB12b N12 slave_latch kQb='kQb'
x12_13 VDD VSS QA13b WE12CLK WE12CLKb RA12 RB12 QB13b N13 slave_latch kQb='kQb'
x12_14 VDD VSS QA14b WE12CLK WE12CLKb RA12 RB12 QB14b N14 slave_latch kQb='kQb'
x12_15 VDD VSS QA15b WE12CLK WE12CLKb RA12 RB12 QB15b N15 slave_latch kQb='kQb'
x13_0 VDD VSS QA0b WE13CLK WE13CLKb RA13 RB13 QB0b N0 slave_latch kQb='kQb'
x13_1 VDD VSS QA1b WE13CLK WE13CLKb RA13 RB13 QB1b N1 slave_latch kQb='kQb'
x13_2 VDD VSS QA2b WE13CLK WE13CLKb RA13 RB13 QB2b N2 slave_latch kQb='kQb'
x13_3 VDD VSS QA3b WE13CLK WE13CLKb RA13 RB13 QB3b N3 slave_latch kQb='kQb'
x13_4 VDD VSS QA4b WE13CLK WE13CLKb RA13 RB13 QB4b N4 slave_latch kQb='kQb'
x13_5 VDD VSS QA5b WE13CLK WE13CLKb RA13 RB13 QB5b N5 slave_latch kQb='kQb'
x13_6 VDD VSS QA6b WE13CLK WE13CLKb RA13 RB13 QB6b N6 slave_latch kQb='kQb'
x13_7 VDD VSS QA7b WE13CLK WE13CLKb RA13 RB13 QB7b N7 slave_latch kQb='kQb'
x13_8 VDD VSS QA8b WE13CLK WE13CLKb RA13 RB13 QB8b N8 slave_latch kQb='kQb'
x13_9 VDD VSS QA9b WE13CLK WE13CLKb RA13 RB13 QB9b N9 slave_latch kQb='kQb'
x13_10 VDD VSS QA10b WE13CLK WE13CLKb RA13 RB13 QB10b N10 slave_latch kQb='kQb'
x13_11 VDD VSS QA11b WE13CLK WE13CLKb RA13 RB13 QB11b N11 slave_latch kQb='kQb'
x13_12 VDD VSS QA12b WE13CLK WE13CLKb RA13 RB13 QB12b N12 slave_latch kQb='kQb'
x13_13 VDD VSS QA13b WE13CLK WE13CLKb RA13 RB13 QB13b N13 slave_latch kQb='kQb'
x13_14 VDD VSS QA14b WE13CLK WE13CLKb RA13 RB13 QB14b N14 slave_latch kQb='kQb'
x13_15 VDD VSS QA15b WE13CLK WE13CLKb RA13 RB13 QB15b N15 slave_latch kQb='kQb'
x14_0 VDD VSS QA0b WE14CLK WE14CLKb RA14 RB14 QB0b N0 slave_latch kQb='kQb'
x14_1 VDD VSS QA1b WE14CLK WE14CLKb RA14 RB14 QB1b N1 slave_latch kQb='kQb'
x14_2 VDD VSS QA2b WE14CLK WE14CLKb RA14 RB14 QB2b N2 slave_latch kQb='kQb'
x14_3 VDD VSS QA3b WE14CLK WE14CLKb RA14 RB14 QB3b N3 slave_latch kQb='kQb'
x14_4 VDD VSS QA4b WE14CLK WE14CLKb RA14 RB14 QB4b N4 slave_latch kQb='kQb'
x14_5 VDD VSS QA5b WE14CLK WE14CLKb RA14 RB14 QB5b N5 slave_latch kQb='kQb'
x14_6 VDD VSS QA6b WE14CLK WE14CLKb RA14 RB14 QB6b N6 slave_latch kQb='kQb'
x14_7 VDD VSS QA7b WE14CLK WE14CLKb RA14 RB14 QB7b N7 slave_latch kQb='kQb'
x14_8 VDD VSS QA8b WE14CLK WE14CLKb RA14 RB14 QB8b N8 slave_latch kQb='kQb'
x14_9 VDD VSS QA9b WE14CLK WE14CLKb RA14 RB14 QB9b N9 slave_latch kQb='kQb'
x14_10 VDD VSS QA10b WE14CLK WE14CLKb RA14 RB14 QB10b N10 slave_latch kQb='kQb'
x14_11 VDD VSS QA11b WE14CLK WE14CLKb RA14 RB14 QB11b N11 slave_latch kQb='kQb'
x14_12 VDD VSS QA12b WE14CLK WE14CLKb RA14 RB14 QB12b N12 slave_latch kQb='kQb'
x14_13 VDD VSS QA13b WE14CLK WE14CLKb RA14 RB14 QB13b N13 slave_latch kQb='kQb'
x14_14 VDD VSS QA14b WE14CLK WE14CLKb RA14 RB14 QB14b N14 slave_latch kQb='kQb'
x14_15 VDD VSS QA15b WE14CLK WE14CLKb RA14 RB14 QB15b N15 slave_latch kQb='kQb'
x15_0 VDD VSS QA0b WE15CLK WE15CLKb RA15 RB15 QB0b N0 slave_latch kQb='kQb'
x15_1 VDD VSS QA1b WE15CLK WE15CLKb RA15 RB15 QB1b N1 slave_latch kQb='kQb'
x15_2 VDD VSS QA2b WE15CLK WE15CLKb RA15 RB15 QB2b N2 slave_latch kQb='kQb'
x15_3 VDD VSS QA3b WE15CLK WE15CLKb RA15 RB15 QB3b N3 slave_latch kQb='kQb'
x15_4 VDD VSS QA4b WE15CLK WE15CLKb RA15 RB15 QB4b N4 slave_latch kQb='kQb'
x15_5 VDD VSS QA5b WE15CLK WE15CLKb RA15 RB15 QB5b N5 slave_latch kQb='kQb'
x15_6 VDD VSS QA6b WE15CLK WE15CLKb RA15 RB15 QB6b N6 slave_latch kQb='kQb'
x15_7 VDD VSS QA7b WE15CLK WE15CLKb RA15 RB15 QB7b N7 slave_latch kQb='kQb'
x15_8 VDD VSS QA8b WE15CLK WE15CLKb RA15 RB15 QB8b N8 slave_latch kQb='kQb'
x15_9 VDD VSS QA9b WE15CLK WE15CLKb RA15 RB15 QB9b N9 slave_latch kQb='kQb'
x15_10 VDD VSS QA10b WE15CLK WE15CLKb RA15 RB15 QB10b N10 slave_latch kQb='kQb'
x15_11 VDD VSS QA11b WE15CLK WE15CLKb RA15 RB15 QB11b N11 slave_latch kQb='kQb'
x15_12 VDD VSS QA12b WE15CLK WE15CLKb RA15 RB15 QB12b N12 slave_latch kQb='kQb'
x15_13 VDD VSS QA13b WE15CLK WE15CLKb RA15 RB15 QB13b N13 slave_latch kQb='kQb'
x15_14 VDD VSS QA14b WE15CLK WE15CLKb RA15 RB15 QB14b N14 slave_latch kQb='kQb'
x15_15 VDD VSS QA15b WE15CLK WE15CLKb RA15 RB15 QB15b N15 slave_latch kQb='kQb'
x1 VDD VSS N0 WEM WEMb D0 master_latch kN='kN'
x2 VDD VSS N1 WEM WEMb D1 master_latch kN='kN'
x3 VDD VSS N2 WEM WEMb D2 master_latch kN='kN'
x4 VDD VSS N3 WEM WEMb D3 master_latch kN='kN'
x5 VDD VSS N4 WEM WEMb D4 master_latch kN='kN'
x6 VDD VSS N5 WEM WEMb D5 master_latch kN='kN'
x7 VDD VSS N6 WEM WEMb D6 master_latch kN='kN'
x8 VDD VSS N7 WEM WEMb D7 master_latch kN='kN'
x9 VDD VSS N8 WEM WEMb D8 master_latch kN='kN'
x10 VDD VSS N9 WEM WEMb D9 master_latch kN='kN'
x11 VDD VSS N10 WEM WEMb D10 master_latch kN='kN'
x12 VDD VSS N11 WEM WEMb D11 master_latch kN='kN'
x13 VDD VSS N12 WEM WEMb D12 master_latch kN='kN'
x14 VDD VSS N13 WEM WEMb D13 master_latch kN='kN'
x15 VDD VSS N14 WEM WEMb D14 master_latch kN='kN'
x16 VDD VSS N15 WEM WEMb D15 master_latch kN='kN'
x17 CLK WE15 WE15CLKb VDD VSS WE15CLK driver_cell kWECLK='kWECLK' kWECLKb='kWECLKb'
x18 CLK WE14 WE14CLKb VDD VSS WE14CLK driver_cell kWECLK='kWECLK' kWECLKb='kWECLKb'
x19 CLK WE13 WE13CLKb VDD VSS WE13CLK driver_cell kWECLK='kWECLK' kWECLKb='kWECLKb'
x20 CLK WE12 WE12CLKb VDD VSS WE12CLK driver_cell kWECLK='kWECLK' kWECLKb='kWECLKb'
x21 CLK WE11 WE11CLKb VDD VSS WE11CLK driver_cell kWECLK='kWECLK' kWECLKb='kWECLKb'
x22 CLK WE10 WE10CLKb VDD VSS WE10CLK driver_cell kWECLK='kWECLK' kWECLKb='kWECLKb'
x23 CLK WE9 WE9CLKb VDD VSS WE9CLK driver_cell kWECLK='kWECLK' kWECLKb='kWECLKb'
x24 CLK WE8 WE8CLKb VDD VSS WE8CLK driver_cell kWECLK='kWECLK' kWECLKb='kWECLKb'
x25 CLK WE7 WE7CLKb VDD VSS WE7CLK driver_cell kWECLK='kWECLK' kWECLKb='kWECLKb'
x26 CLK WE6 WE6CLKb VDD VSS WE6CLK driver_cell kWECLK='kWECLK' kWECLKb='kWECLKb'
x27 CLK WE5 WE5CLKb VDD VSS WE5CLK driver_cell kWECLK='kWECLK' kWECLKb='kWECLKb'
x28 CLK WE4 WE4CLKb VDD VSS WE4CLK driver_cell kWECLK='kWECLK' kWECLKb='kWECLKb'
x29 CLK WE3 WE3CLKb VDD VSS WE3CLK driver_cell kWECLK='kWECLK' kWECLKb='kWECLKb'
x30 CLK WE2 WE2CLKb VDD VSS WE2CLK driver_cell kWECLK='kWECLK' kWECLKb='kWECLKb'
x31 CLK WE1 WE1CLKb VDD VSS WE1CLK driver_cell kWECLK='kWECLK' kWECLKb='kWECLKb'
x32 CLK WE0 WE0CLKb VDD VSS WE0CLK driver_cell kWECLK='kWECLK' kWECLKb='kWECLKb'
x33 VDD VSS QA0 QA0b QB0b QB0 output_inverter
x34 VDD VSS QA1 QA1b QB1b QB1 output_inverter
x35 VDD VSS QA2 QA2b QB2b QB2 output_inverter
x36 VDD VSS QA3 QA3b QB3b QB3 output_inverter
x37 VDD VSS QA4 QA4b QB4b QB4 output_inverter
x38 VDD VSS QA5 QA5b QB5b QB5 output_inverter
x39 VDD VSS QA6 QA6b QB6b QB6 output_inverter
x40 VDD VSS QA7 QA7b QB7b QB7 output_inverter
x41 VDD VSS QA8 QA8b QB8b QB8 output_inverter
x42 VDD VSS QA9 QA9b QB9b QB9 output_inverter
x43 VDD VSS QA10 QA10b QB10b QB10 output_inverter
x44 VDD VSS QA11 QA11b QB11b QB11 output_inverter
x45 VDD VSS QA12 QA12b QB12b QB12 output_inverter
x46 VDD VSS QA13 QA13b QB13b QB13 output_inverter
x47 VDD VSS QA14 QA14b QB14b QB14 output_inverter
x48 VDD VSS QA15 QA15b QB15b QB15 output_inverter
x49 VDD WEM WEMb VSS wem_inverter
**** begin user architecture code


.param kWECLKb=1.34/0.36
.param kWECLK=1.27/0.36
.param kWEMb=1.26/0.36
.param kQb=0.36/0.36
.param kN=1.24/0.36


**** end user architecture code
**.ends

* expanding   symbol:  engn1600-team1/CAD3/slave_latch.sym # of pins=9
** sym_path: CAD3/slave_latch.sym
** sch_path: CAD3/slave_latch.sch
.subckt slave_latch VDD VSS QA WECLK WECLKb RA RB QB D  kQb=1
*.ipin D
*.ipin RA
*.ipin RB
*.ipin WECLKb
*.ipin WECLK
*.opin QA
*.opin QB
*.iopin VDD
*.iopin VSS
XM1 net1 WECLKb net2 VDD pfet_03v3 L=0.28u W=0.22u nf=1 ad='int((nf+1)/2) * W/nf * 0.18u' as='int((nf+2)/2) * W/nf * 0.18u'
+ pd='2*int((nf+1)/2) * (W/nf + 0.18u)' ps='2*int((nf+2)/2) * (W/nf + 0.18u)' nrd='0.18u / W' nrs='0.18u / W'
+ sa=0 sb=0 sd=0 m=1
XM2 net1 D VDD VDD pfet_03v3 L=0.28u W=0.22u nf=1 ad='int((nf+1)/2) * W/nf * 0.18u' as='int((nf+2)/2) * W/nf * 0.18u'
+ pd='2*int((nf+1)/2) * (W/nf + 0.18u)' ps='2*int((nf+2)/2) * (W/nf + 0.18u)' nrd='0.18u / W' nrs='0.18u / W'
+ sa=0 sb=0 sd=0 m=1
XM3 net3 net2 VDD VDD pfet_03v3 L=0.28u W=0.22u nf=1 ad='int((nf+1)/2) * W/nf * 0.18u' as='int((nf+2)/2) * W/nf * 0.18u'
+ pd='2*int((nf+1)/2) * (W/nf + 0.18u)' ps='2*int((nf+2)/2) * (W/nf + 0.18u)' nrd='0.18u / W' nrs='0.18u / W'
+ sa=0 sb=0 sd=0 m=1
XM4 net4 net2 VDD VDD pfet_03v3 L=0.28u W=0.22u nf=1 ad='int((nf+1)/2) * W/nf * 0.18u' as='int((nf+2)/2) * W/nf * 0.18u'
+ pd='2*int((nf+1)/2) * (W/nf + 0.18u)' ps='2*int((nf+2)/2) * (W/nf + 0.18u)' nrd='0.18u / W' nrs='0.18u / W'
+ sa=0 sb=0 sd=0 m=1
XM5 VDD WECLK net8 VDD pfet_03v3 L=0.28u W=0.22u nf=1 ad='int((nf+1)/2) * W/nf * 0.18u' as='int((nf+2)/2) * W/nf * 0.18u'
+ pd='2*int((nf+1)/2) * (W/nf + 0.18u)' ps='2*int((nf+2)/2) * (W/nf + 0.18u)' nrd='0.18u / W' nrs='0.18u / W'
+ sa=0 sb=0 sd=0 m=1
XM6 net8 net4 net2 VDD pfet_03v3 L=0.28u W=0.22u nf=1 ad='int((nf+1)/2) * W/nf * 0.18u' as='int((nf+2)/2) * W/nf * 0.18u'
+ pd='2*int((nf+1)/2) * (W/nf + 0.18u)' ps='2*int((nf+2)/2) * (W/nf + 0.18u)' nrd='0.18u / W' nrs='0.18u / W'
+ sa=0 sb=0 sd=0 m=1
XM7 net1 D VSS VSS nfet_03v3 L=0.28u W=0.22u nf=1 ad='int((nf+1)/2) * W/nf * 0.18u' as='int((nf+2)/2) * W/nf * 0.18u'
+ pd='2*int((nf+1)/2) * (W/nf + 0.18u)' ps='2*int((nf+2)/2) * (W/nf + 0.18u)' nrd='0.18u / W' nrs='0.18u / W'
+ sa=0 sb=0 sd=0 m=1
XM8 net1 WECLK net2 VSS nfet_03v3 L=0.28u W=0.22u nf=1 ad='int((nf+1)/2) * W/nf * 0.18u' as='int((nf+2)/2) * W/nf * 0.18u'
+ pd='2*int((nf+1)/2) * (W/nf + 0.18u)' ps='2*int((nf+2)/2) * (W/nf + 0.18u)' nrd='0.18u / W' nrs='0.18u / W'
+ sa=0 sb=0 sd=0 m=1
XM9 net3 net2 VSS VSS nfet_03v3 L=0.28u W=0.22u nf=1 ad='int((nf+1)/2) * W/nf * 0.18u' as='int((nf+2)/2) * W/nf * 0.18u'
+ pd='2*int((nf+1)/2) * (W/nf + 0.18u)' ps='2*int((nf+2)/2) * (W/nf + 0.18u)' nrd='0.18u / W' nrs='0.18u / W'
+ sa=0 sb=0 sd=0 m=1
XM10 net4 net2 VSS VSS nfet_03v3 L=0.28u W=0.22u nf=1 ad='int((nf+1)/2) * W/nf * 0.18u' as='int((nf+2)/2) * W/nf * 0.18u'
+ pd='2*int((nf+1)/2) * (W/nf + 0.18u)' ps='2*int((nf+2)/2) * (W/nf + 0.18u)' nrd='0.18u / W' nrs='0.18u / W'
+ sa=0 sb=0 sd=0 m=1
XM11 net7 net4 net2 VSS nfet_03v3 L=0.28u W=0.22u nf=1 ad='int((nf+1)/2) * W/nf * 0.18u' as='int((nf+2)/2) * W/nf * 0.18u'
+ pd='2*int((nf+1)/2) * (W/nf + 0.18u)' ps='2*int((nf+2)/2) * (W/nf + 0.18u)' nrd='0.18u / W' nrs='0.18u / W'
+ sa=0 sb=0 sd=0 m=1
XM12 VSS WECLKb net7 VSS nfet_03v3 L=0.28u W=0.22u nf=1 ad='int((nf+1)/2) * W/nf * 0.18u' as='int((nf+2)/2) * W/nf * 0.18u'
+ pd='2*int((nf+1)/2) * (W/nf + 0.18u)' ps='2*int((nf+2)/2) * (W/nf + 0.18u)' nrd='0.18u / W' nrs='0.18u / W'
+ sa=0 sb=0 sd=0 m=1
XM13 net3 net5 QB VDD pfet_03v3 L=0.28u W=0.22u nf=1 ad='int((nf+1)/2) * W/nf * 0.18u' as='int((nf+2)/2) * W/nf * 0.18u'
+ pd='2*int((nf+1)/2) * (W/nf + 0.18u)' ps='2*int((nf+2)/2) * (W/nf + 0.18u)' nrd='0.18u / W' nrs='0.18u / W'
+ sa=0 sb=0 sd=0 m=1
XM14 net3 RB QB VSS nfet_03v3 L=0.28u W=0.22u nf=1 ad='int((nf+1)/2) * W/nf * 0.18u' as='int((nf+2)/2) * W/nf * 0.18u'
+ pd='2*int((nf+1)/2) * (W/nf + 0.18u)' ps='2*int((nf+2)/2) * (W/nf + 0.18u)' nrd='0.18u / W' nrs='0.18u / W'
+ sa=0 sb=0 sd=0 m=1
XM15 net5 RB VDD VDD pfet_03v3 L=0.28u W=0.22u nf=1 ad='int((nf+1)/2) * W/nf * 0.18u' as='int((nf+2)/2) * W/nf * 0.18u'
+ pd='2*int((nf+1)/2) * (W/nf + 0.18u)' ps='2*int((nf+2)/2) * (W/nf + 0.18u)' nrd='0.18u / W' nrs='0.18u / W'
+ sa=0 sb=0 sd=0 m=1
XM16 net5 RB VSS VSS nfet_03v3 L=0.28u W=0.22u nf=1 ad='int((nf+1)/2) * W/nf * 0.18u' as='int((nf+2)/2) * W/nf * 0.18u'
+ pd='2*int((nf+1)/2) * (W/nf + 0.18u)' ps='2*int((nf+2)/2) * (W/nf + 0.18u)' nrd='0.18u / W' nrs='0.18u / W'
+ sa=0 sb=0 sd=0 m=1
XM21 net3 net6 QA VDD pfet_03v3 L=0.28u W=0.22u nf=1 ad='int((nf+1)/2) * W/nf * 0.18u' as='int((nf+2)/2) * W/nf * 0.18u'
+ pd='2*int((nf+1)/2) * (W/nf + 0.18u)' ps='2*int((nf+2)/2) * (W/nf + 0.18u)' nrd='0.18u / W' nrs='0.18u / W'
+ sa=0 sb=0 sd=0 m=1
XM22 net3 RA QA VSS nfet_03v3 L=0.28u W=0.22u nf=1 ad='int((nf+1)/2) * W/nf * 0.18u' as='int((nf+2)/2) * W/nf * 0.18u'
+ pd='2*int((nf+1)/2) * (W/nf + 0.18u)' ps='2*int((nf+2)/2) * (W/nf + 0.18u)' nrd='0.18u / W' nrs='0.18u / W'
+ sa=0 sb=0 sd=0 m=1
XM23 net6 RA VDD VDD pfet_03v3 L=0.28u W=0.22u nf=1 ad='int((nf+1)/2) * W/nf * 0.18u' as='int((nf+2)/2) * W/nf * 0.18u'
+ pd='2*int((nf+1)/2) * (W/nf + 0.18u)' ps='2*int((nf+2)/2) * (W/nf + 0.18u)' nrd='0.18u / W' nrs='0.18u / W'
+ sa=0 sb=0 sd=0 m=1
XM24 net6 RA VSS VSS nfet_03v3 L=0.28u W=0.22u nf=1 ad='int((nf+1)/2) * W/nf * 0.18u' as='int((nf+2)/2) * W/nf * 0.18u'
+ pd='2*int((nf+1)/2) * (W/nf + 0.18u)' ps='2*int((nf+2)/2) * (W/nf + 0.18u)' nrd='0.18u / W' nrs='0.18u / W'
+ sa=0 sb=0 sd=0 m=1
.ends


* expanding   symbol:  engn1600-team1/CAD3/master_latch.sym # of pins=6
** sym_path: CAD3/master_latch.sym
** sch_path: CAD3/master_latch.sch
.subckt master_latch VDD VSS Q WEM WEMb D  kN=1
*.ipin D
*.ipin WEMb
*.ipin WEM
*.iopin VSS
*.iopin VDD
*.opin Q
XM3 net1 WEMb net2 VDD pfet_03v3 L=0.28u W=0.36u nf=1 ad='int((nf+1)/2) * W/nf * 0.18u' as='int((nf+2)/2) * W/nf * 0.18u'
+ pd='2*int((nf+1)/2) * (W/nf + 0.18u)' ps='2*int((nf+2)/2) * (W/nf + 0.18u)' nrd='0.18u / W' nrs='0.18u / W'
+ sa=0 sb=0 sd=0 m=1
XM7 net1 D VDD VDD pfet_03v3 L=0.28u W=0.72u nf=1 ad='int((nf+1)/2) * W/nf * 0.18u' as='int((nf+2)/2) * W/nf * 0.18u'
+ pd='2*int((nf+1)/2) * (W/nf + 0.18u)' ps='2*int((nf+2)/2) * (W/nf + 0.18u)' nrd='0.18u / W' nrs='0.18u / W'
+ sa=0 sb=0 sd=0 m=1
XM8 Q net2 VDD VDD pfet_03v3 L=0.28u W=0.72u nf=4 ad='int((nf+1)/2) * W/nf * 0.18u' as='int((nf+2)/2) * W/nf * 0.18u'
+ pd='2*int((nf+1)/2) * (W/nf + 0.18u)' ps='2*int((nf+2)/2) * (W/nf + 0.18u)' nrd='0.18u / W' nrs='0.18u / W'
+ sa=0 sb=0 sd=0 m=1
XM9 net3 net2 VDD VDD pfet_03v3 L=0.28u W=0.36u nf=1 ad='int((nf+1)/2) * W/nf * 0.18u' as='int((nf+2)/2) * W/nf * 0.18u'
+ pd='2*int((nf+1)/2) * (W/nf + 0.18u)' ps='2*int((nf+2)/2) * (W/nf + 0.18u)' nrd='0.18u / W' nrs='0.18u / W'
+ sa=0 sb=0 sd=0 m=1
XM10 VDD WEM net5 VDD pfet_03v3 L=0.28u W=0.36u nf=1 ad='int((nf+1)/2) * W/nf * 0.18u' as='int((nf+2)/2) * W/nf * 0.18u'
+ pd='2*int((nf+1)/2) * (W/nf + 0.18u)' ps='2*int((nf+2)/2) * (W/nf + 0.18u)' nrd='0.18u / W' nrs='0.18u / W'
+ sa=0 sb=0 sd=0 m=1
XM12 net5 net3 net2 VDD pfet_03v3 L=0.28u W=0.36u nf=1 ad='int((nf+1)/2) * W/nf * 0.18u' as='int((nf+2)/2) * W/nf * 0.18u'
+ pd='2*int((nf+1)/2) * (W/nf + 0.18u)' ps='2*int((nf+2)/2) * (W/nf + 0.18u)' nrd='0.18u / W' nrs='0.18u / W'
+ sa=0 sb=0 sd=0 m=1
XM19 net1 D VSS VSS nfet_03v3 L=0.28u W=0.36u nf=1 ad='int((nf+1)/2) * W/nf * 0.18u' as='int((nf+2)/2) * W/nf * 0.18u'
+ pd='2*int((nf+1)/2) * (W/nf + 0.18u)' ps='2*int((nf+2)/2) * (W/nf + 0.18u)' nrd='0.18u / W' nrs='0.18u / W'
+ sa=0 sb=0 sd=0 m=1
XM20 net1 WEM net2 VSS nfet_03v3 L=0.28u W=0.36u nf=1 ad='int((nf+1)/2) * W/nf * 0.18u' as='int((nf+2)/2) * W/nf * 0.18u'
+ pd='2*int((nf+1)/2) * (W/nf + 0.18u)' ps='2*int((nf+2)/2) * (W/nf + 0.18u)' nrd='0.18u / W' nrs='0.18u / W'
+ sa=0 sb=0 sd=0 m=1
XM21 Q net2 VSS VSS nfet_03v3 L=0.28u W=0.36u nf=4 ad='int((nf+1)/2) * W/nf * 0.18u' as='int((nf+2)/2) * W/nf * 0.18u'
+ pd='2*int((nf+1)/2) * (W/nf + 0.18u)' ps='2*int((nf+2)/2) * (W/nf + 0.18u)' nrd='0.18u / W' nrs='0.18u / W'
+ sa=0 sb=0 sd=0 m=1
XM22 net3 net2 VSS VSS nfet_03v3 L=0.28u W=0.36u nf=1 ad='int((nf+1)/2) * W/nf * 0.18u' as='int((nf+2)/2) * W/nf * 0.18u'
+ pd='2*int((nf+1)/2) * (W/nf + 0.18u)' ps='2*int((nf+2)/2) * (W/nf + 0.18u)' nrd='0.18u / W' nrs='0.18u / W'
+ sa=0 sb=0 sd=0 m=1
XM23 net4 net3 net2 VSS nfet_03v3 L=0.28u W=0.36u nf=1 ad='int((nf+1)/2) * W/nf * 0.18u' as='int((nf+2)/2) * W/nf * 0.18u'
+ pd='2*int((nf+1)/2) * (W/nf + 0.18u)' ps='2*int((nf+2)/2) * (W/nf + 0.18u)' nrd='0.18u / W' nrs='0.18u / W'
+ sa=0 sb=0 sd=0 m=1
XM24 VSS WEMb net4 VSS nfet_03v3 L=0.28u W=0.36u nf=1 ad='int((nf+1)/2) * W/nf * 0.18u' as='int((nf+2)/2) * W/nf * 0.18u'
+ pd='2*int((nf+1)/2) * (W/nf + 0.18u)' ps='2*int((nf+2)/2) * (W/nf + 0.18u)' nrd='0.18u / W' nrs='0.18u / W'
+ sa=0 sb=0 sd=0 m=1
.ends


* expanding   symbol:  engn1600-team1/CAD3/driver_cell.sym # of pins=6
** sym_path: CAD3/driver_cell.sym
** sch_path: CAD3/driver_cell.sch
.subckt driver_cell CLK WE WECLKb VDD VSS WECLK  kWECLK=1 kWECLKb=1
*.ipin CLK
*.ipin WE
*.iopin VSS
*.iopin VDD
*.opin WECLKb
*.opin WECLK
XM13 WECLK net1 VDD VDD pfet_03v3 L=0.28u W=2.54u nf=1 ad='int((nf+1)/2) * W/nf * 0.18u' as='int((nf+2)/2) * W/nf * 0.18u'
+ pd='2*int((nf+1)/2) * (W/nf + 0.18u)' ps='2*int((nf+2)/2) * (W/nf + 0.18u)' nrd='0.18u / W' nrs='0.18u / W'
+ sa=0 sb=0 sd=0 m=1
XM14 WECLK net1 VSS VSS nfet_03v3 L=0.28u W=1.27u nf=1 ad='int((nf+1)/2) * W/nf * 0.18u' as='int((nf+2)/2) * W/nf * 0.18u'
+ pd='2*int((nf+1)/2) * (W/nf + 0.18u)' ps='2*int((nf+2)/2) * (W/nf + 0.18u)' nrd='0.18u / W' nrs='0.18u / W'
+ sa=0 sb=0 sd=0 m=1
XM1 WECLKb WECLK VDD VDD pfet_03v3 L=0.28u W=2.68u nf=1 ad='int((nf+1)/2) * W/nf * 0.18u' as='int((nf+2)/2) * W/nf * 0.18u'
+ pd='2*int((nf+1)/2) * (W/nf + 0.18u)' ps='2*int((nf+2)/2) * (W/nf + 0.18u)' nrd='0.18u / W' nrs='0.18u / W'
+ sa=0 sb=0 sd=0 m=1
XM2 WECLKb WECLK VSS VSS nfet_03v3 L=0.28u W=1.34u nf=1 ad='int((nf+1)/2) * W/nf * 0.18u' as='int((nf+2)/2) * W/nf * 0.18u'
+ pd='2*int((nf+1)/2) * (W/nf + 0.18u)' ps='2*int((nf+2)/2) * (W/nf + 0.18u)' nrd='0.18u / W' nrs='0.18u / W'
+ sa=0 sb=0 sd=0 m=1
XM3 net1 CLK VDD VDD pfet_03v3 L=0.28u W=0.72u nf=1 ad='int((nf+1)/2) * W/nf * 0.18u' as='int((nf+2)/2) * W/nf * 0.18u'
+ pd='2*int((nf+1)/2) * (W/nf + 0.18u)' ps='2*int((nf+2)/2) * (W/nf + 0.18u)' nrd='0.18u / W' nrs='0.18u / W'
+ sa=0 sb=0 sd=0 m=1
XM4 net1 WE VDD VDD pfet_03v3 L=0.28u W=0.72u nf=1 ad='int((nf+1)/2) * W/nf * 0.18u' as='int((nf+2)/2) * W/nf * 0.18u'
+ pd='2*int((nf+1)/2) * (W/nf + 0.18u)' ps='2*int((nf+2)/2) * (W/nf + 0.18u)' nrd='0.18u / W' nrs='0.18u / W'
+ sa=0 sb=0 sd=0 m=1
XM5 net2 WE VSS VSS nfet_03v3 L=0.28u W=0.72u nf=1 ad='int((nf+1)/2) * W/nf * 0.18u' as='int((nf+2)/2) * W/nf * 0.18u'
+ pd='2*int((nf+1)/2) * (W/nf + 0.18u)' ps='2*int((nf+2)/2) * (W/nf + 0.18u)' nrd='0.18u / W' nrs='0.18u / W'
+ sa=0 sb=0 sd=0 m=1
XM6 net1 CLK net2 VSS nfet_03v3 L=0.28u W=0.72u nf=1 ad='int((nf+1)/2) * W/nf * 0.18u' as='int((nf+2)/2) * W/nf * 0.18u'
+ pd='2*int((nf+1)/2) * (W/nf + 0.18u)' ps='2*int((nf+2)/2) * (W/nf + 0.18u)' nrd='0.18u / W' nrs='0.18u / W'
+ sa=0 sb=0 sd=0 m=1
.ends


* expanding   symbol:  engn1600-team1/CAD3/output_inverter.sym # of pins=6
** sym_path: CAD3/output_inverter.sym
** sch_path: CAD3/output_inverter.sch
.subckt output_inverter VDD VSS QAb QA QB QBb
*.opin QB
*.opin QA
*.iopin VDD
*.iopin VSS
*.ipin QAb
*.ipin QBb
XM3 QB QBb VDD VDD pfet_03v3 L=0.28u W=0.72u nf=1 ad='int((nf+1)/2) * W/nf * 0.18u' as='int((nf+2)/2) * W/nf * 0.18u'
+ pd='2*int((nf+1)/2) * (W/nf + 0.18u)' ps='2*int((nf+2)/2) * (W/nf + 0.18u)' nrd='0.18u / W' nrs='0.18u / W'
+ sa=0 sb=0 sd=0 m=1
XM4 QB QBb VSS VSS nfet_03v3 L=0.28u W=0.36 nf=1 ad='int((nf+1)/2) * W/nf * 0.18u' as='int((nf+2)/2) * W/nf * 0.18u'
+ pd='2*int((nf+1)/2) * (W/nf + 0.18u)' ps='2*int((nf+2)/2) * (W/nf + 0.18u)' nrd='0.18u / W' nrs='0.18u / W'
+ sa=0 sb=0 sd=0 m=1
XM35 QA QAb VDD VDD pfet_03v3 L=0.28u W=0.72u nf=1 ad='int((nf+1)/2) * W/nf * 0.18u' as='int((nf+2)/2) * W/nf * 0.18u'
+ pd='2*int((nf+1)/2) * (W/nf + 0.18u)' ps='2*int((nf+2)/2) * (W/nf + 0.18u)' nrd='0.18u / W' nrs='0.18u / W'
+ sa=0 sb=0 sd=0 m=1
XM36 QA QAb VSS VSS nfet_03v3 L=0.28u W=0.36u nf=1 ad='int((nf+1)/2) * W/nf * 0.18u' as='int((nf+2)/2) * W/nf * 0.18u'
+ pd='2*int((nf+1)/2) * (W/nf + 0.18u)' ps='2*int((nf+2)/2) * (W/nf + 0.18u)' nrd='0.18u / W' nrs='0.18u / W'
+ sa=0 sb=0 sd=0 m=1
.ends


* expanding   symbol:  engn1600-team1/CAD3/wem_inverter.sym # of pins=4
** sym_path: CAD3/wem_inverter.sym
** sch_path: CAD3/wem_inverter.sch
.subckt wem_inverter VDD WEM WEMb VSS
*.ipin WEM
*.opin WEMb
*.iopin VDD
*.iopin VSS
XM1 WEMb WEM VDD VDD pfet_03v3 L=0.28u W='kWEMb*0.72u' nf=1 ad='int((nf+1)/2) * W/nf * 0.18u' as='int((nf+2)/2) * W/nf * 0.18u'
+ pd='2*int((nf+1)/2) * (W/nf + 0.18u)' ps='2*int((nf+2)/2) * (W/nf + 0.18u)' nrd='0.18u / W' nrs='0.18u / W'
+ sa=0 sb=0 sd=0 m=1
XM2 WEMb WEM VSS VSS nfet_03v3 L=0.28u W='kWEMb*0.36u' nf=1 ad='int((nf+1)/2) * W/nf * 0.18u' as='int((nf+2)/2) * W/nf * 0.18u'
+ pd='2*int((nf+1)/2) * (W/nf + 0.18u)' ps='2*int((nf+2)/2) * (W/nf + 0.18u)' nrd='0.18u / W' nrs='0.18u / W'
+ sa=0 sb=0 sd=0 m=1
**** begin user architecture code


.param kWEMb=1


**** end user architecture code
.ends

.end
